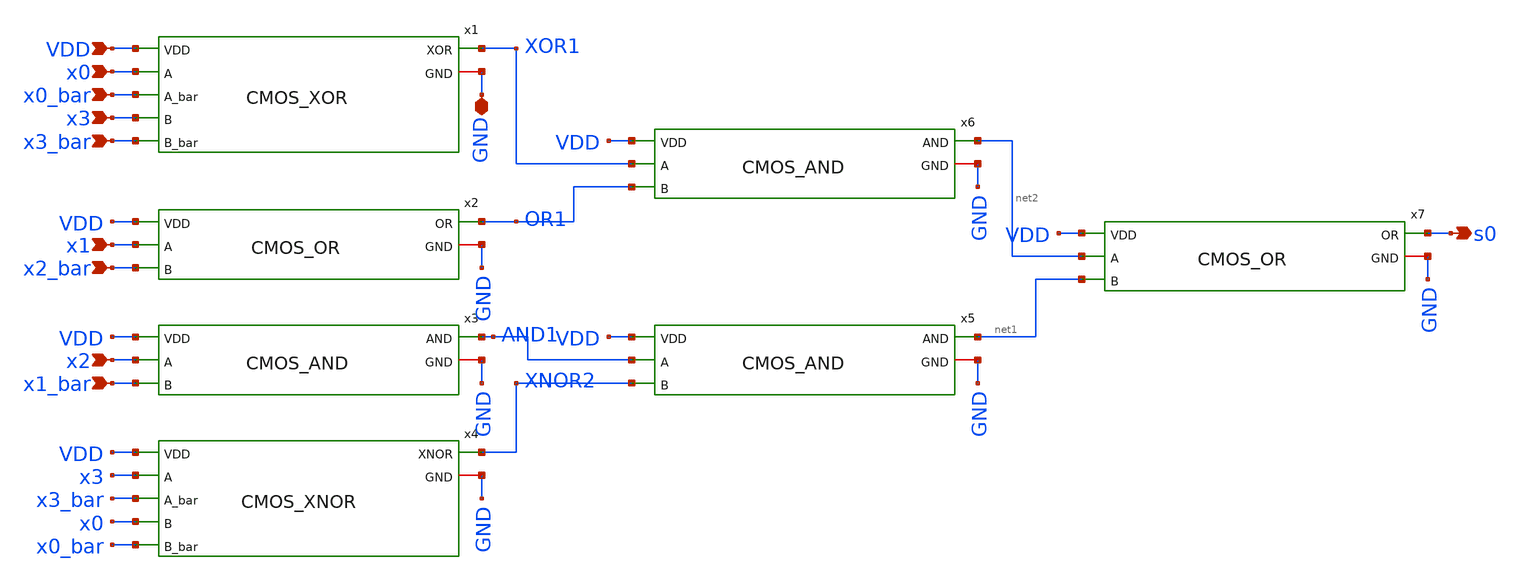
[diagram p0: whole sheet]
** sch_path: skywater_stuff/CMOS_s0.sch
**.subckt CMOS_s0 GND x0 x0_bar x1 x1_bar x2 x2_bar x3 x3_bar VDD s0
*.iopin GND
*.ipin x0
*.ipin x0_bar
*.ipin x1
*.ipin x1_bar
*.ipin x2
*.ipin x2_bar
*.ipin x3
*.ipin x3_bar
*.ipin VDD
*.opin s0
x4 x3 x3_bar x0 x0_bar XNOR2 GND VDD CMOS_XNOR
x5 AND1 XNOR2 net1 GND VDD CMOS_AND
x6 XOR1 OR1 net2 GND VDD CMOS_AND
x7 net2 net1 s0 GND VDD CMOS_OR
x1 x0 x0_bar x3 x3_bar XOR1 GND VDD CMOS_XOR
x2 x1 x2_bar OR1 GND VDD CMOS_OR
x3 x2 x1_bar AND1 GND VDD CMOS_AND
**.ends
.end
